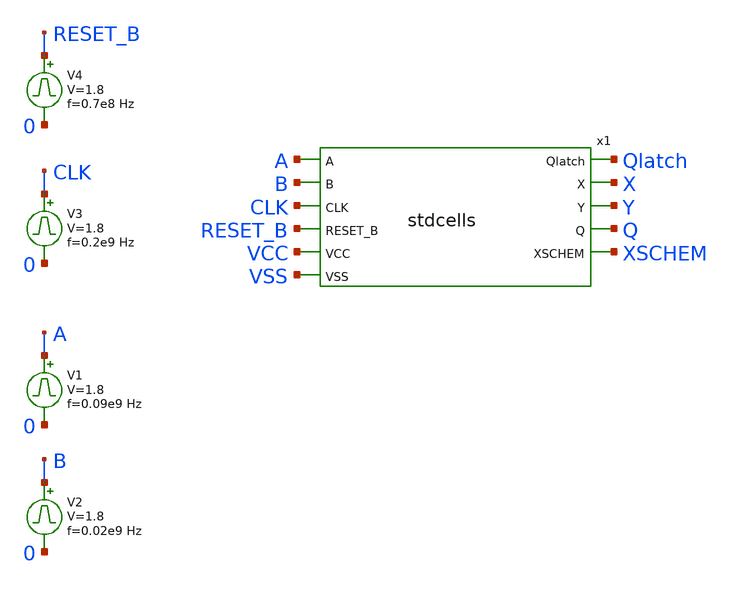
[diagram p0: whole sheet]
** sch_path: sky130_tests/test_stdcells.sch
* Copyright 2021 Stefan Frederik Schippers
* Licensed under the Apache License, Version 2.0 (the "License");
* you may not use this file except in compliance with the License.
* You may obtain a copy of the License at
* https://www.apache.org/licenses/LICENSE-2.0
* Unless required by applicable law or agreed to in writing, software
* distributed under the License is distributed on an "AS IS" BASIS,
* WITHOUT WARRANTIES OR CONDITIONS OF ANY KIND, either express or implied.
* See the License for the specific language governing permissions and
* limitations under the License.
.lib $::SKYWATER_MODELS/sky130.lib.spice tt
.include $::SKYWATER_STDCELLS/sky130_fd_sc_hd.spice

**.subckt test_stdcells
V1 A 0 pulse 0 1.8 '0.495/ 0.09e9 ' '0.01/0.09e9 ' '0.01/0.09e9 ' '0.49/0.09e9 ' '1/0.09e9 '
V2 B 0 pulse 0 1.8 '0.495/ 0.02e9 ' '0.01/0.02e9 ' '0.01/0.02e9 ' '0.49/0.02e9 ' '1/0.02e9 '
V3 CLK 0 pulse 0 1.8 '0.495/ 0.2e9 ' '0.01/0.2e9 ' '0.01/0.2e9 ' '0.49/0.2e9 ' '1/0.2e9 '
V4 RESET_B 0 pulse 0 1.8 '0.495/ 0.7e8 ' '0.01/0.7e8 ' '0.01/0.7e8 ' '0.49/0.7e8 ' '1/0.7e8 '
x1 Qlatch A X B Y CLK Q RESET_B XSCHEM VCC VSS stdcells
**** begin user architecture code


.options acct list
.temp 25
vvcc vcc 0 dc 1.8
vvss vss 0 0
.control
tran 30p 80n
plot a b+2 clk+4 reset_b+6 x+8 y+10 q+12 qlatch+14
write test_stdcells.raw
.endc


**** end user architecture code
**.ends

* expanding   symbol:  sky130_tests/stdcells.sym # of pins=11
** sym_path: sky130_tests/stdcells.sym
** sch_path: sky130_tests/stdcells.sch
.subckt stdcells Qlatch A X B Y CLK Q RESET_B XSCHEM VCC VSS
*.ipin RESET_B
*.ipin CLK
*.ipin B
*.ipin A
*.opin Y
*.opin X
*.opin Qlatch
*.opin Q
*.opin XSCHEM
*.ipin VCC
*.ipin VSS
x1 A B VSS VSS VCC VCC X sky130_fd_sc_hd__nand2_1
C1 X 0 3f m=1
x2 CLK A RESET_B VSS VSS VCC VCC Q sky130_fd_sc_hd__dfrtp_1
C2 Q 0 3f m=1
C3 Y 0 3f m=1
x3 A B VSS VSS VCC VCC Y sky130_fd_sc_hd__nor2b_1
x4 A CLK RESET_B VSS VSS VCC VCC Qlatch net1 sky130_fd_sc_hd__dlrbn_1
C4 Qlatch 0 3f m=1
x5 Y B VSS VSS VCC VCC net2 sky130_fd_sc_hd__nor2b_1
x6 net2 Qlatch VSS VSS VCC VCC net4 sky130_fd_sc_hd__nand2_1
x7 net3 net4 Q RESET_B VSS VSS VCC VCC XSCHEM sky130_fd_sc_hd__a31o_2
* noconn #net1
* noconn XSCHEM
x8 Y VSS VSS VCC VCC net3 sky130_fd_sc_hd__inv_2
.ends

.end
